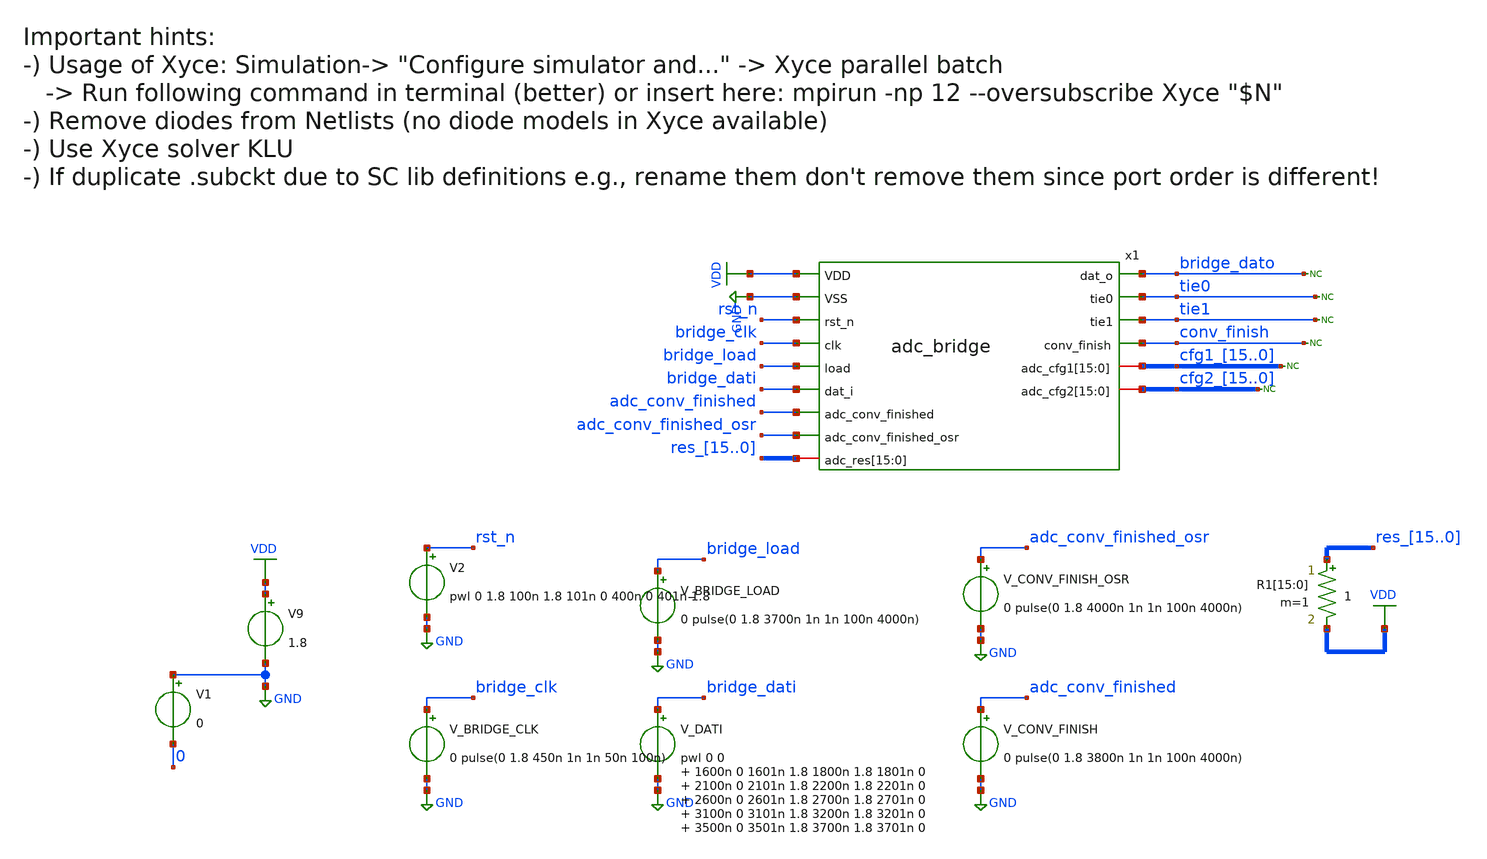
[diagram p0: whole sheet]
** sch_path: xschem/adc_bridge_tb.sch
**.subckt adc_bridge_tb
V_DATI bridge_dati GND pwl 0 0 1600n 0 1601n 1.8 1800n 1.8 1801n 0 2100n 0 2101n 1.8 2200n 1.8 2201n
+ 0 2600n 0 2601n 1.8 2700n 1.8 2701n 0 3100n 0 3101n 1.8 3200n 1.8 3201n 0 3500n 0 3501n 1.8 3700n 1.8
+ 3701n 0
V_BRIDGE_LOAD bridge_load GND 0 pulse(0 1.8 3700n 1n 1n 100n 4000n)
V9 VDD GND 1.8
V_CONV_FINISH_OSR adc_conv_finished_osr GND 0 pulse(0 1.8 4000n 1n 1n 100n 4000n)
V_CONV_FINISH adc_conv_finished GND 0 pulse(0 1.8 3800n 1n 1n 100n 4000n)
x1 VDD GND rst_n bridge_clk bridge_load bridge_dati bridge_dato tie0 tie1 adc_conv_finished
+ adc_conv_finished_osr conv_finish cfg1_15 cfg1_14 cfg1_13 cfg1_12 cfg1_11 cfg1_10 cfg1_9 cfg1_8 cfg1_7 cfg1_6 cfg1_5
+ cfg1_4 cfg1_3 cfg1_2 cfg1_1 cfg1_0 cfg2_15 cfg2_14 cfg2_13 cfg2_12 cfg2_11 cfg2_10 cfg2_9 cfg2_8 cfg2_7
+ cfg2_6 cfg2_5 cfg2_4 cfg2_3 cfg2_2 cfg2_1 cfg2_0 res_15 res_14 res_13 res_12 res_11 res_10 res_9 res_8
+ res_7 res_6 res_5 res_4 res_3 res_2 res_1 res_0 adc_bridge
R1[15] res_15 VDD 1 m=1
R1[14] res_14 VDD 1 m=1
R1[13] res_13 VDD 1 m=1
R1[12] res_12 VDD 1 m=1
R1[11] res_11 VDD 1 m=1
R1[10] res_10 VDD 1 m=1
R1[9] res_9 VDD 1 m=1
R1[8] res_8 VDD 1 m=1
R1[7] res_7 VDD 1 m=1
R1[6] res_6 VDD 1 m=1
R1[5] res_5 VDD 1 m=1
R1[4] res_4 VDD 1 m=1
R1[3] res_3 VDD 1 m=1
R1[2] res_2 VDD 1 m=1
R1[1] res_1 VDD 1 m=1
R1[0] res_0 VDD 1 m=1
V1 GND 0 0
V_BRIDGE_CLK bridge_clk GND 0 pulse(0 1.8 450n 1n 1n 50n 100n)
V2 rst_n GND pwl 0 1.8 100n 1.8 101n 0 400n 0 401n 1.8
* noconn bridge_dato
* noconn tie0
* noconn tie1
* noconn conv_finish
* noconn cfg1_[15..0]
* noconn cfg2_[15..0]
**** begin user architecture code

** opencircuitdesign pdks install
.lib $::SKYWATER_MODELS/sky130.lib.spice tt





* ngspice commands

.include /foss/designs/sky130_adc_202311/xschem/adc_bridge_sim.spice

.save all
.control
.option reltol=0.01
.option gmin=1.0e-10
.option rshunt=1.0e10
set num_threads=11
tran 5n 5.5u

write adc_bridge_tb.raw

.endc






**** end user architecture code
**.ends
.GLOBAL VDD
.GLOBAL GND
.end
